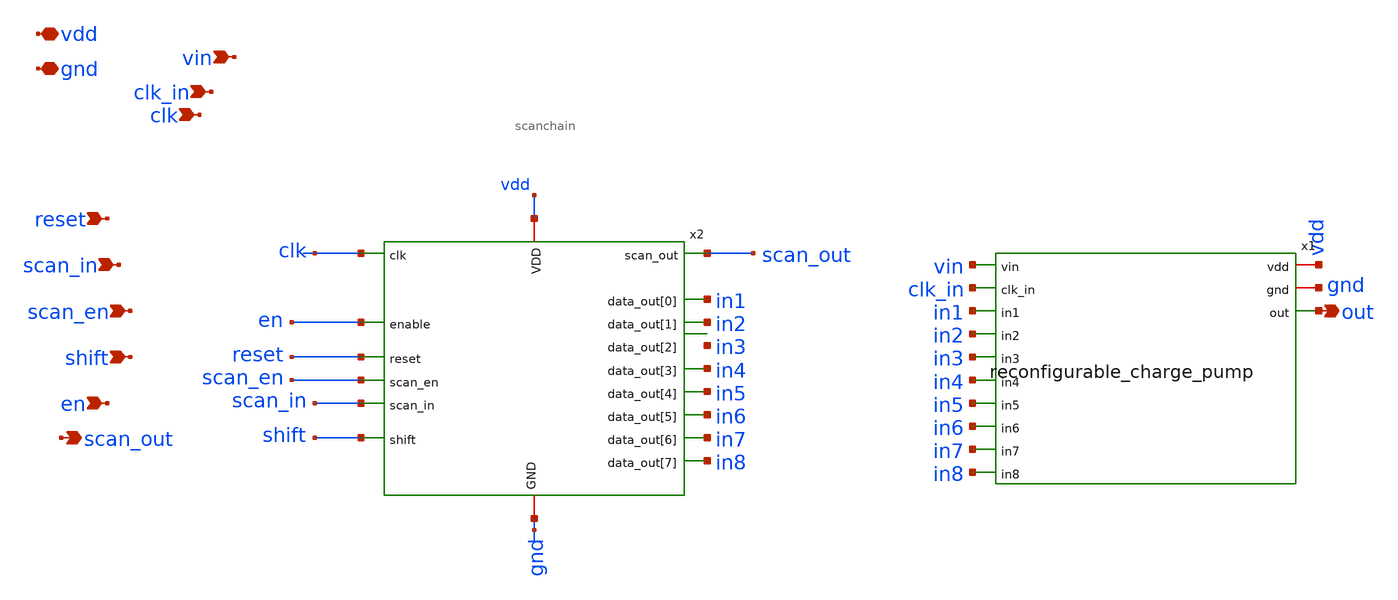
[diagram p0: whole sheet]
** sch_path: xschem/charge_pumps2/reconfigurable_CP_withScanchain2.sch
**.subckt reconfigurable_CP_withScanchain2 gnd vdd vin clk_in clk reset scan_in scan_en shift en out
*+ scan_out
*.iopin gnd
*.iopin vdd
*.ipin vin
*.ipin clk_in
*.ipin clk
*.ipin reset
*.ipin scan_in
*.ipin scan_en
*.ipin shift
*.ipin en
*.opin out
*.opin scan_out
x2 gnd vdd clk in1 in2 in3 in4 in5 in6 in7 in8 en reset scan_en scan_in scan_out shift scanchain
x1 vin clk_in vdd gnd in1 in2 in3 in4 in5 in6 in7 in8 out reconfigurable_charge_pump
**.ends
.end
